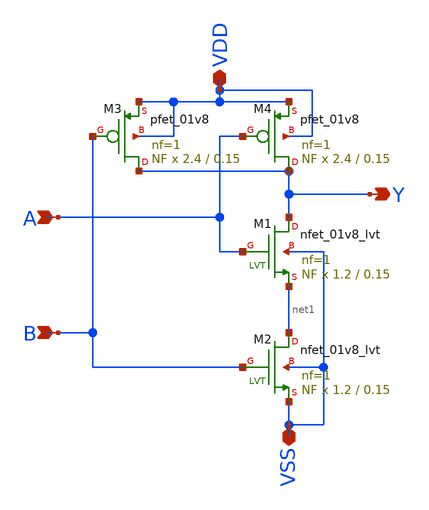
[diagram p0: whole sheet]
** sch_path: xschem_lib/sylee21/nand.sch
**.subckt nand Y A VDD VSS B
*.opin Y
*.ipin A
*.iopin VDD
*.iopin VSS
*.ipin B
XM1 Y A net1 VSS sky130_fd_pr__nfet_01v8_lvt L=0.15 W=1.2 nf=1 ad='int((nf+1)/2) * W/nf * 0.29' as='int((nf+2)/2) * W/nf * 0.29'
+ pd='2*int((nf+1)/2) * (W/nf + 0.29)' ps='2*int((nf+2)/2) * (W/nf + 0.29)' nrd='0.29 / W' nrs='0.29 / W'
+ sa=0 sb=0 sd=0 mult=NF m=NF
XM2 net1 B VSS VSS sky130_fd_pr__nfet_01v8_lvt L=0.15 W=1.2 nf=1 ad='int((nf+1)/2) * W/nf * 0.29' as='int((nf+2)/2) * W/nf * 0.29'
+ pd='2*int((nf+1)/2) * (W/nf + 0.29)' ps='2*int((nf+2)/2) * (W/nf + 0.29)' nrd='0.29 / W' nrs='0.29 / W'
+ sa=0 sb=0 sd=0 mult=NF m=NF
XM3 Y B VDD VDD sky130_fd_pr__pfet_01v8 L=0.15 W=2.4 nf=1 ad='int((nf+1)/2) * W/nf * 0.29' as='int((nf+2)/2) * W/nf * 0.29'
+ pd='2*int((nf+1)/2) * (W/nf + 0.29)' ps='2*int((nf+2)/2) * (W/nf + 0.29)' nrd='0.29 / W' nrs='0.29 / W'
+ sa=0 sb=0 sd=0 mult=NF m=NF
XM4 Y A VDD VDD sky130_fd_pr__pfet_01v8 L=0.15 W=2.4 nf=1 ad='int((nf+1)/2) * W/nf * 0.29' as='int((nf+2)/2) * W/nf * 0.29'
+ pd='2*int((nf+1)/2) * (W/nf + 0.29)' ps='2*int((nf+2)/2) * (W/nf + 0.29)' nrd='0.29 / W' nrs='0.29 / W'
+ sa=0 sb=0 sd=0 mult=NF m=NF
**.ends
.end
